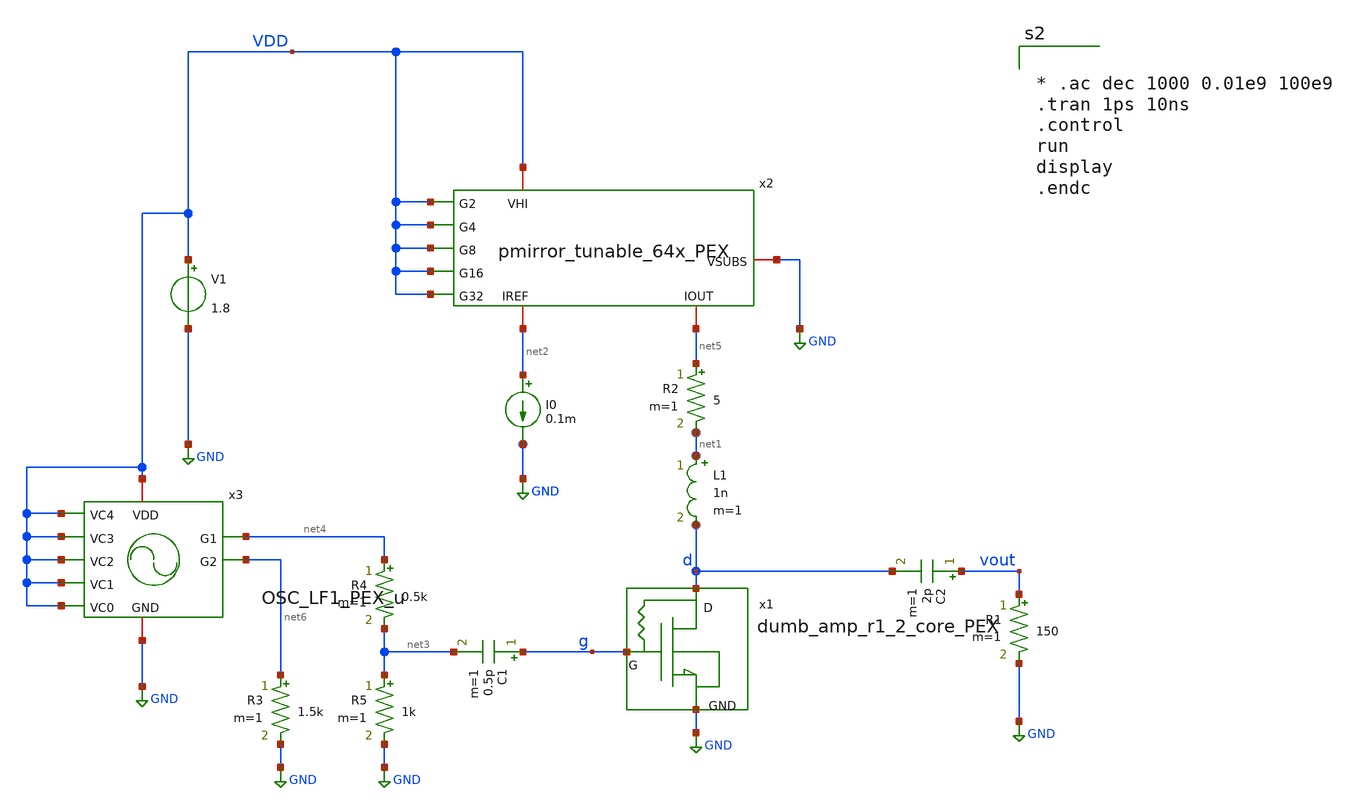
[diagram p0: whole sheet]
** sch_path: xschem/dumb_amp_r1_2_PEX_tran.sch
**.subckt dumb_amp_r1_2_PEX_tran
V1 VDD GND 1.8
C2 vout d 2p m=1
L1 net1 d 1n m=1
R2 net5 net1 5 m=1
I0 net2 GND 0.1m
R1 vout GND 150 m=1
R4 net4 net3 0.5k m=1
R5 net3 GND 1k m=1
x1 g d GND dumb_amp_r1_2_core_PEX
x2 VDD VDD VDD GND VDD net2 net5 VDD VDD pmirror_tunable_64x_PEX
C1 g net3 0.5p m=1
x3 VDD VDD net4 net6 VDD VDD VDD VDD GND OSC_LF1_PEX_u
R3 net6 GND 1.5k m=1
**** begin user architecture code
.lib $::SKYWATER_MODELS/sky130.lib.spice tt
* .include $::PDKPATH/libs.ref/sky130_fd_sc_hvl/spice/sky130_fd_sc_hvl.spice



* .ac dec 1000 0.01e9 100e9
.tran 1ps 10ns
.control
run
display
.endc


**** end user architecture code
**.ends

* expanding   symbol:  dumb_amp_r1_2_core_PEX.sym # of pins=3
** sym_path: xschem/dumb_amp_r1_2_core_PEX.sym
** sch_path: xschem/dumb_amp_r1_2_core_PEX.sch
.subckt dumb_amp_r1_2_core_PEX G D GND
*.iopin G
*.iopin D
*.iopin GND
**** begin user architecture code

.subckt dumb_amp_core_pex NGATE NDRAIN VSUBS
.subckt sky130_fd_pr__rf_nfet_01v8_aM02W5p00L0p15 DRAIN GATE SOURCE SUBSTRATE
X0 DRAIN GATE SOURCE SUBSTRATE sky130_fd_pr__nfet_01v8 ad=1.414e+12p pd=1.066e+07u as=2.828e+12p
+ ps=2.132e+07u w=5.05e+06u l=150000u
X1 SOURCE GATE DRAIN SUBSTRATE sky130_fd_pr__nfet_01v8 ad=0p pd=0u as=0p ps=0u w=5.05e+06u l=150000u
C0 DRAIN SOURCE 3.59fF
C1 GATE SOURCE 0.46fF
C2 DRAIN GATE 0.34fF
C3 DRAIN SUBSTRATE 0.40fF
C4 SOURCE SUBSTRATE 2.44fF
C5 GATE SUBSTRATE 0.64fF
.ends
.subckt nfet_3x_2 D G S sub
Xsky130_fd_pr__rf_nfet_01v8_aM02W5p00L0p15_0 D G S sub sky130_fd_pr__rf_nfet_01v8_aM02W5p00L0p15
Xsky130_fd_pr__rf_nfet_01v8_aM02W5p00L0p15_1 D G S sub sky130_fd_pr__rf_nfet_01v8_aM02W5p00L0p15
Xsky130_fd_pr__rf_nfet_01v8_aM02W5p00L0p15_2 D G S sub sky130_fd_pr__rf_nfet_01v8_aM02W5p00L0p15
C0 G sub 1.34fF
C1 S D -0.11fF
C2 S G 2.13fF
C3 G D 1.69fF
C4 S sub -0.01fF
C5 D sub -0.05fF
C6 sub 0 -1.34fF
C7 D 0 0.62fF
C8 S 0 6.66fF
C9 G 0 1.96fF
.ends
.subckt RF_nfet_6xaM02W5p0L0p15 G S D B
Xnfet_3x_2_0 D G S B nfet_3x_2
Xnfet_3x_2_1 D G S B nfet_3x_2
C0 D B -0.02fF
C1 G S 0.20fF
C2 G B 0.06fF
C3 G D 0.14fF
C4 S B 0.02fF
C5 D S 0.01fF
C6 B 0 -3.73fF
C7 D 0 1.02fF
C8 S 0 13.03fF
C9 G 0 3.30fF
.ends
.subckt sky130_fd_pr__res_generic_po_JFYRVD a_75_284# a_n141_n357# a_n271_n487#
R0 a_n141_n357# a_75_284# sky130_fd_pr__res_generic_po w=330000u l=6.2e+06u
C0 a_n141_n357# a_n271_n487# 0.14fF
C1 a_75_284# a_n271_n487# 0.14fF
.ends
XRF_nfet_6xaM02W5p0L0p15_0 NGATE NDRAIN VSUBS VSUBS RF_nfet_6xaM02W5p0L0p15
Xsky130_fd_pr__res_generic_po_JFYRVD_0 NGATE NDRAIN VSUBS sky130_fd_pr__res_generic_po_JFYRVD
C0 VSUBS NDRAIN 1.42fF
C1 NGATE VSUBS 2.81fF
C2 NGATE NDRAIN 2.91fF
C5 NDRAIN VSUBS 14.22fF
C6 NGATE VSUBS 3.28fF
.ends

XDUT G D GND dumb_amp_core_pex


**** end user architecture code
.ends


* expanding   symbol:  pmirror_tunable_64x_PEX.sym # of pins=9
** sym_path: xschem/pmirror_tunable_64x_PEX.sym
** sch_path: xschem/pmirror_tunable_64x_PEX.sch
.subckt pmirror_tunable_64x_PEX VHI G2 G4 VSUBS G8 IREF IOUT G16 G32
*.ipin G2
*.ipin G4
*.ipin G8
*.ipin G16
*.ipin G32
*.iopin VHI
*.iopin VSUBS
*.iopin IREF
*.iopin IOUT
**** begin user architecture code

* SPICE3 file created from pmirror_pfet_64x_complete.ext - technology: sky130B
X0 pmirror_pfet_64x_flat_0/G32 IREF VSUBS sky130_fd_pr__res_xhigh_po_0p35 l=500000u
X1 pmirror_pfet_64x_flat_0/G4  IREF VSUBS sky130_fd_pr__res_xhigh_po_0p35 l=500000u
X2 pmirror_pfet_64x_flat_0/G8  IREF VSUBS sky130_fd_pr__res_xhigh_po_0p35 l=500000u
X3 pmirror_pfet_64x_flat_0/G2  IREF VSUBS sky130_fd_pr__res_xhigh_po_0p35 l=500000u
X5 pmirror_pfet_64x_flat_0/G16 IREF VSUBS sky130_fd_pr__res_xhigh_po_0p35 l=500000u

X7 VHI pmirror_pfet_64x_flat_0/G32 IOUT VHI sky130_fd_pr__pfet_01v8 ad=0p pd=0u as=0p ps=0u w=1e+06u
+ l=300000u
X8 IOUT pmirror_pfet_64x_flat_0/G32 VHI VHI sky130_fd_pr__pfet_01v8 ad=0p pd=0u as=0p ps=0u w=1e+06u
+ l=300000u
X11 IOUT pmirror_pfet_64x_flat_0/G32 VHI VHI sky130_fd_pr__pfet_01v8 ad=0p pd=0u as=0p ps=0u
+ w=1e+06u l=300000u
X16 VHI pmirror_pfet_64x_flat_0/G32 IOUT VHI sky130_fd_pr__pfet_01v8 ad=0p pd=0u as=0p ps=0u
+ w=1e+06u l=300000u
X17 VHI pmirror_pfet_64x_flat_0/G32 IOUT VHI sky130_fd_pr__pfet_01v8 ad=0p pd=0u as=0p ps=0u
+ w=1e+06u l=300000u
X18 VHI pmirror_pfet_64x_flat_0/G32 IOUT VHI sky130_fd_pr__pfet_01v8 ad=0p pd=0u as=0p ps=0u
+ w=1e+06u l=300000u
X21 IOUT pmirror_pfet_64x_flat_0/G32 VHI VHI sky130_fd_pr__pfet_01v8 ad=0p pd=0u as=0p ps=0u
+ w=1e+06u l=300000u
X22 IOUT pmirror_pfet_64x_flat_0/G32 VHI VHI sky130_fd_pr__pfet_01v8 ad=0p pd=0u as=0p ps=0u
+ w=1e+06u l=300000u
X27 IOUT pmirror_pfet_64x_flat_0/G32 VHI VHI sky130_fd_pr__pfet_01v8 ad=1p pd=0u as=0p ps=0u
+ w=1e+06u l=300000u
X28 IOUT pmirror_pfet_64x_flat_0/G32 VHI VHI sky130_fd_pr__pfet_01v8 ad=0p pd=0u as=0p ps=0u
+ w=1e+06u l=300000u
X29 VHI pmirror_pfet_64x_flat_0/G32 IOUT VHI sky130_fd_pr__pfet_01v8 ad=0p pd=0u as=0p ps=0u
+ w=1e+06u l=300000u
X25 VHI pmirror_pfet_64x_flat_0/G32 IOUT VHI sky130_fd_pr__pfet_01v8 ad=0p pd=0u as=0p ps=0u
+ w=1e+06u l=300000u
X35 VHI pmirror_pfet_64x_flat_0/G32 IOUT VHI sky130_fd_pr__pfet_01v8 ad=0p pd=0u as=0p ps=0u
+ w=1e+06u l=300000u
X38 VHI pmirror_pfet_64x_flat_0/G32 IOUT VHI sky130_fd_pr__pfet_01v8 ad=0p pd=0u as=0p ps=0u
+ w=1e+06u l=300000u
X41 VHI pmirror_pfet_64x_flat_0/G32 IOUT VHI sky130_fd_pr__pfet_01v8 ad=0p pd=0u as=0p ps=0u
+ w=1e+06u l=300000u
X43 IOUT pmirror_pfet_64x_flat_0/G32 VHI VHI sky130_fd_pr__pfet_01v8 ad=0p pd=0u as=0p ps=0u
+ w=1e+06u l=300000u
X44 IOUT pmirror_pfet_64x_flat_0/G32 VHI VHI sky130_fd_pr__pfet_01v8 ad=0p pd=0u as=0p ps=0u
+ w=1e+06u l=300000u
X46 VHI pmirror_pfet_64x_flat_0/G32 IOUT VHI sky130_fd_pr__pfet_01v8 ad=0p pd=0u as=0p ps=0u
+ w=1e+06u l=300000u
X54 VHI pmirror_pfet_64x_flat_0/G32 IOUT VHI sky130_fd_pr__pfet_01v8 ad=0p pd=0u as=0p ps=0u
+ w=1e+06u l=300000u
X55 IOUT pmirror_pfet_64x_flat_0/G32 VHI VHI sky130_fd_pr__pfet_01v8 ad=0p pd=0u as=0p ps=0u
+ w=1e+06u l=300000u
X56 IOUT pmirror_pfet_64x_flat_0/G32 VHI VHI sky130_fd_pr__pfet_01v8 ad=0p pd=0u as=0p ps=0u
+ w=1e+06u l=300000u
X60 IOUT pmirror_pfet_64x_flat_0/G32 VHI VHI sky130_fd_pr__pfet_01v8 ad=0p pd=0u as=0p ps=0u
+ w=1e+06u l=300000u
X61 IOUT pmirror_pfet_64x_flat_0/G32 VHI VHI sky130_fd_pr__pfet_01v8 ad=0p pd=0u as=0p ps=0u
+ w=1e+06u l=300000u
X62 VHI pmirror_pfet_64x_flat_0/G32 IOUT VHI sky130_fd_pr__pfet_01v8 ad=0p pd=0u as=0p ps=0u
+ w=1e+06u l=300000u
X67 IOUT pmirror_pfet_64x_flat_0/G32 VHI VHI sky130_fd_pr__pfet_01v8 ad=0p pd=0u as=0p ps=0u
+ w=1e+06u l=300000u
X68 IOUT pmirror_pfet_64x_flat_0/G32 VHI VHI sky130_fd_pr__pfet_01v8 ad=0p pd=0u as=0p ps=0u
+ w=1e+06u l=300000u
X50 VHI pmirror_pfet_64x_flat_0/G32 IOUT VHI sky130_fd_pr__pfet_01v8 ad=0p pd=0u as=0p ps=0u
+ w=1e+06u l=300000u
X73 VHI pmirror_pfet_64x_flat_0/G32 IOUT VHI sky130_fd_pr__pfet_01v8 ad=0p pd=0u as=0p ps=0u
+ w=1e+06u l=300000u
X74 IOUT pmirror_pfet_64x_flat_0/G32 VHI VHI sky130_fd_pr__pfet_01v8 ad=0p pd=0u as=0p ps=0u
+ w=1e+06u l=300000u
X75 IOUT pmirror_pfet_64x_flat_0/G32 VHI VHI sky130_fd_pr__pfet_01v8 ad=0p pd=0u as=0p ps=0u
+ w=1e+06u l=300000u
X69 VHI pmirror_pfet_64x_flat_0/G32 IOUT VHI sky130_fd_pr__pfet_01v8 ad=0p pd=0u as=0p ps=0u
+ w=1e+06u l=300000u
X81 VHI pmirror_pfet_64x_flat_0/G32 IOUT VHI sky130_fd_pr__pfet_01v8 ad=0p pd=0u as=0p ps=0u
+ w=1e+06u l=300000u

X49 VHI VHI IOUT VHI sky130_fd_pr__pfet_01v8 ad=0p pd=0u as=0p ps=0u w=1e+06u l=300000u
X79 IREF IREF VHI VHI sky130_fd_pr__pfet_01v8 ad=0p pd=0u as=0p ps=0u w=1e+06u l=300000u

X6 IOUT pmirror_pfet_64x_flat_0/G16 VHI VHI sky130_fd_pr__pfet_01v8 ad=0p pd=0u as=0p ps=0u w=1e+06u
+ l=300000u
X9 VHI pmirror_pfet_64x_flat_0/G16 IOUT VHI sky130_fd_pr__pfet_01v8 ad=0p pd=0u as=0p ps=0u w=1e+06u
+ l=300000u
X10 IOUT pmirror_pfet_64x_flat_0/G16 VHI VHI sky130_fd_pr__pfet_01v8 ad=0p pd=0u as=0p ps=0u
+ w=1e+06u l=300000u
X19 IOUT pmirror_pfet_64x_flat_0/G16 VHI VHI sky130_fd_pr__pfet_01v8 ad=0p pd=0u as=0p ps=0u
+ w=1e+06u l=300000u
X20 IOUT pmirror_pfet_64x_flat_0/G16 VHI VHI sky130_fd_pr__pfet_01v8 ad=0p pd=0u as=0p ps=0u
+ w=1e+06u l=300000u
X26 VHI pmirror_pfet_64x_flat_0/G16 IOUT VHI sky130_fd_pr__pfet_01v8 ad=0p pd=0u as=0p ps=0u
+ w=1e+06u l=300000u
X30 IOUT pmirror_pfet_64x_flat_0/G16 VHI VHI sky130_fd_pr__pfet_01v8 ad=0p pd=0u as=0p ps=0u
+ w=1e+06u l=300000u
X33 IOUT pmirror_pfet_64x_flat_0/G16 VHI VHI sky130_fd_pr__pfet_01v8 ad=0p pd=0u as=0p ps=0u
+ w=1e+06u l=300000u
X36 VHI pmirror_pfet_64x_flat_0/G16 IOUT VHI sky130_fd_pr__pfet_01v8 ad=0p pd=0u as=0p ps=0u
+ w=1e+06u l=300000u
X45 VHI pmirror_pfet_64x_flat_0/G16 IOUT VHI sky130_fd_pr__pfet_01v8 ad=0p pd=0u as=0p ps=0u
+ w=1e+06u l=300000u
X53 VHI pmirror_pfet_64x_flat_0/G16 IOUT VHI sky130_fd_pr__pfet_01v8 ad=0p pd=0u as=0p ps=0u
+ w=1e+06u l=300000u
X57 VHI pmirror_pfet_64x_flat_0/G16 IOUT VHI sky130_fd_pr__pfet_01v8 ad=0p pd=0u as=0p ps=0u
+ w=1e+06u l=300000u
X58 VHI pmirror_pfet_64x_flat_0/G16 IOUT VHI sky130_fd_pr__pfet_01v8 ad=0p pd=0u as=0p ps=0u
+ w=1e+06u l=300000u
X65 VHI pmirror_pfet_64x_flat_0/G16 IOUT VHI sky130_fd_pr__pfet_01v8 ad=0p pd=0u as=0p ps=0u
+ w=1e+06u l=300000u
X82 IOUT pmirror_pfet_64x_flat_0/G16 VHI VHI sky130_fd_pr__pfet_01v8 ad=0p pd=0u as=0p ps=0u
+ w=1e+06u l=300000u
X83 IOUT pmirror_pfet_64x_flat_0/G16 VHI VHI sky130_fd_pr__pfet_01v8 ad=0p pd=0u as=0p ps=0u
+ w=1e+06u l=300000u

X14 IOUT pmirror_pfet_64x_flat_0/G8 VHI VHI sky130_fd_pr__pfet_01v8 ad=0p pd=0u as=0p ps=0u w=1e+06u
+ l=300000u
X23 VHI pmirror_pfet_64x_flat_0/G8 IOUT VHI sky130_fd_pr__pfet_01v8 ad=0p pd=0u as=0p ps=0u w=1e+06u
+ l=300000u
X31 VHI pmirror_pfet_64x_flat_0/G8 IOUT VHI sky130_fd_pr__pfet_01v8 ad=0p pd=0u as=0p ps=0u w=1e+06u
+ l=300000u
X32 VHI pmirror_pfet_64x_flat_0/G8 IOUT VHI sky130_fd_pr__pfet_01v8 ad=0p pd=0u as=0p ps=0u w=1e+06u
+ l=300000u
X42 VHI pmirror_pfet_64x_flat_0/G8 IOUT VHI sky130_fd_pr__pfet_01v8 ad=0p pd=0u as=0p ps=0u w=1e+06u
+ l=300000u
X72 IOUT pmirror_pfet_64x_flat_0/G8 VHI VHI sky130_fd_pr__pfet_01v8 ad=0p pd=0u as=0p ps=0u w=1e+06u
+ l=300000u
X80 IOUT pmirror_pfet_64x_flat_0/G8 VHI VHI sky130_fd_pr__pfet_01v8 ad=0p pd=0u as=0p ps=0u w=1e+06u
+ l=300000u
X84 IOUT pmirror_pfet_64x_flat_0/G8 VHI VHI sky130_fd_pr__pfet_01v8 ad=0p pd=0u as=0p ps=0u w=1e+06u
+ l=300000u

X85 IOUT pmirror_pfet_64x_flat_0/G4 VHI VHI sky130_fd_pr__pfet_01v8 ad=0p pd=0u as=0p ps=0u w=1e+06u
+ l=300000u
X39 VHI pmirror_pfet_64x_flat_0/G4 IOUT VHI sky130_fd_pr__pfet_01v8 ad=0p pd=0u as=0p ps=0u w=1e+06u
+ l=300000u
X40 VHI pmirror_pfet_64x_flat_0/G4 IOUT VHI sky130_fd_pr__pfet_01v8 ad=0p pd=0u as=0p ps=0u w=1e+06u
+ l=300000u
X70 IOUT pmirror_pfet_64x_flat_0/G4 VHI VHI sky130_fd_pr__pfet_01v8 ad=0p pd=0u as=0p ps=0u w=1e+06u
+ l=300000u

X48 VHI pmirror_pfet_64x_flat_0/G2 IOUT VHI sky130_fd_pr__pfet_01v8 ad=0p pd=0u as=0p ps=0u w=1e+06u
+ l=300000u
X15 IOUT pmirror_pfet_64x_flat_0/G2 VHI VHI sky130_fd_pr__pfet_01v8 ad=0p pd=0u as=0p ps=0u w=1e+06u
+ l=300000u

X86 VHI G32 pmirror_pfet_64x_flat_0/G32 VHI sky130_fd_pr__pfet_01v8 ad=0p pd=0u as=0p ps=0u
+ w=30e+06u l=150000u
X87 VHI G16 pmirror_pfet_64x_flat_0/G16 VHI sky130_fd_pr__pfet_01v8 ad=0p pd=0u as=0p ps=0u
+ w=30e+06u l=150000u
X88 VHI G2 pmirror_pfet_64x_flat_0/G2 VHI sky130_fd_pr__pfet_01v8 ad=0p pd=0u as=0p ps=0u w=30e+06u
+ l=150000u
X89 VHI G4 pmirror_pfet_64x_flat_0/G4 VHI sky130_fd_pr__pfet_01v8 ad=0p pd=0u as=0p ps=0u w=30e+06u
+ l=150000u
X90 VHI G8 pmirror_pfet_64x_flat_0/G8 VHI sky130_fd_pr__pfet_01v8 ad=0p pd=0u as=0p ps=0u w=30e+06u
+ l=150000u

C0 VHI pmirror_pfet_64x_flat_0/G8 10.15fF
C1 pmirror_pfet_64x_flat_0/G16 IOUT 2.36fF
C2 pmirror_pfet_64x_flat_0/G4 VHI 4.30fF
C3 pmirror_pfet_64x_flat_0/G2 IREF 2.13fF
C4 pmirror_pfet_64x_flat_0/G16 pmirror_pfet_64x_flat_0/G8 4.66fF
C5 pmirror_pfet_64x_flat_0/G4 pmirror_pfet_64x_flat_0/G8 3.24fF
C6 pmirror_pfet_64x_flat_0/G2 VHI 4.48fF
C7 pmirror_pfet_64x_flat_0/G4 pmirror_pfet_64x_flat_0/G2 2.55fF
C8 VHI IREF 4.53fF
C9 VHI pmirror_pfet_64x_flat_0/G32 15.40fF
C10 IOUT pmirror_pfet_64x_flat_0/G32 5.39fF
C11 pmirror_pfet_64x_flat_0/G16 pmirror_pfet_64x_flat_0/G32 3.74fF
C12 VHI IOUT 24.04fF
C13 pmirror_pfet_64x_flat_0/G16 VHI 4.93fF
C14 VHI VSUBS 46.10fF


**** end user architecture code
.ends


* expanding   symbol:  OSC_LF1_PEX_u.sym # of pins=9
** sym_path: xschem/OSC_LF1_PEX_u.sym
** sch_path: xschem/OSC_LF1_PEX_u.sch
.subckt OSC_LF1_PEX_u VDD VC4 G1 G2 VC3 VC2 VC1 VC0 GND
*.ipin VC0
*.ipin VC1
*.ipin VC2
*.ipin VC3
*.ipin VC4
*.iopin GND
*.iopin VDD
*.opin G1
*.opin G2
**** begin user architecture code






**** COMPLETE *****

.subckt COMPLETE VH VL I1 I2 G0 G1 G2 G3 G4

.subckt sky130_fd_pr__rf_pfet_01v8_aF04W5p00L0p15 DRAIN GATE SOURCE
X0 DRAIN GATE SOURCE SOURCE sky130_fd_pr__pfet_01v8 ad=2.8e+12p pd=2.112e+07u as=4.05e+12p
+ ps=3.162e+07u w=5e+06u l=150000u
X1 SOURCE GATE DRAIN SOURCE sky130_fd_pr__pfet_01v8 ad=0p pd=0u as=0p ps=0u w=5e+06u l=150000u
X2 SOURCE GATE DRAIN SOURCE sky130_fd_pr__pfet_01v8 ad=0p pd=0u as=0p ps=0u w=5e+06u l=150000u
X3 DRAIN GATE SOURCE SOURCE sky130_fd_pr__pfet_01v8 ad=0p pd=0u as=0p ps=0u w=5e+06u l=150000u
C0 DRAIN SOURCE 6.07fF
.ends

X0 I2 G0 captuner_complete_2_0/sky130_fd_pr__rf_nfet_01v8_aM04W5p00L0p15_fingered_0/S VL
+ sky130_fd_pr__nfet_01v8 ad=0p pd=0u as=0p ps=0u w=5.05e+06u l=150000u
X1 I2 G0 captuner_complete_2_0/sky130_fd_pr__rf_nfet_01v8_aM04W5p00L0p15_fingered_0/S VL
+ sky130_fd_pr__nfet_01v8 ad=0p pd=0u as=0p ps=0u w=5.05e+06u l=150000u
X2 captuner_complete_2_0/sky130_fd_pr__rf_nfet_01v8_aM04W5p00L0p15_fingered_0/S G0 I2 VL
+ sky130_fd_pr__nfet_01v8 ad=0p pd=0u as=0p ps=0u w=5.05e+06u l=150000u
X3 captuner_complete_2_0/sky130_fd_pr__rf_nfet_01v8_aM04W5p00L0p15_fingered_0/S G0 I2 VL
+ sky130_fd_pr__nfet_01v8 ad=0p pd=0u as=0p ps=0u w=5.05e+06u l=150000u
X4 I2 G1 captuner_complete_2_0/sky130_fd_pr__rf_nfet_01v8_aM04W5p00L0p15_fingered_1/S VL
+ sky130_fd_pr__nfet_01v8 ad=0p pd=0u as=0p ps=0u w=5.05e+06u l=150000u
X5 I2 G1 captuner_complete_2_0/sky130_fd_pr__rf_nfet_01v8_aM04W5p00L0p15_fingered_1/S VL
+ sky130_fd_pr__nfet_01v8 ad=0p pd=0u as=0p ps=0u w=5.05e+06u l=150000u
X6 captuner_complete_2_0/sky130_fd_pr__rf_nfet_01v8_aM04W5p00L0p15_fingered_1/S G1 I2 VL
+ sky130_fd_pr__nfet_01v8 ad=0p pd=0u as=0p ps=0u w=5.05e+06u l=150000u
X7 captuner_complete_2_0/sky130_fd_pr__rf_nfet_01v8_aM04W5p00L0p15_fingered_1/S G1 I2 VL
+ sky130_fd_pr__nfet_01v8 ad=0p pd=0u as=0p ps=0u w=5.05e+06u l=150000u
X8 I2 G2 captuner_complete_2_0/sky130_fd_pr__rf_nfet_01v8_aM04W5p00L0p15_fingered_2/S VL
+ sky130_fd_pr__nfet_01v8 ad=0p pd=0u as=0p ps=0u w=5.05e+06u l=150000u
X9 I2 G2 captuner_complete_2_0/sky130_fd_pr__rf_nfet_01v8_aM04W5p00L0p15_fingered_2/S VL
+ sky130_fd_pr__nfet_01v8 ad=0p pd=0u as=0p ps=0u w=5.05e+06u l=150000u
X10 captuner_complete_2_0/sky130_fd_pr__rf_nfet_01v8_aM04W5p00L0p15_fingered_2/S G2 I2 VL
+ sky130_fd_pr__nfet_01v8 ad=0p pd=0u as=0p ps=0u w=5.05e+06u l=150000u
X11 captuner_complete_2_0/sky130_fd_pr__rf_nfet_01v8_aM04W5p00L0p15_fingered_2/S G2 I2 VL
+ sky130_fd_pr__nfet_01v8 ad=0p pd=0u as=0p ps=0u w=5.05e+06u l=150000u
X12 I2 G3 captuner_complete_2_0/sky130_fd_pr__rf_nfet_01v8_aM04W5p00L0p15_fingered_4/S VL
+ sky130_fd_pr__nfet_01v8 ad=0p pd=0u as=0p ps=0u w=5.05e+06u l=150000u
X13 I2 G3 captuner_complete_2_0/sky130_fd_pr__rf_nfet_01v8_aM04W5p00L0p15_fingered_4/S VL
+ sky130_fd_pr__nfet_01v8 ad=0p pd=0u as=0p ps=0u w=5.05e+06u l=150000u
X14 captuner_complete_2_0/sky130_fd_pr__rf_nfet_01v8_aM04W5p00L0p15_fingered_4/S G3 I2 VL
+ sky130_fd_pr__nfet_01v8 ad=0p pd=0u as=0p ps=0u w=5.05e+06u l=150000u
X15 captuner_complete_2_0/sky130_fd_pr__rf_nfet_01v8_aM04W5p00L0p15_fingered_4/S G3 I2 VL
+ sky130_fd_pr__nfet_01v8 ad=0p pd=0u as=0p ps=0u w=5.05e+06u l=150000u
X16 I2 G3 captuner_complete_2_0/sky130_fd_pr__rf_nfet_01v8_aM04W5p00L0p15_fingered_4/S VL
+ sky130_fd_pr__nfet_01v8 ad=0p pd=0u as=0p ps=0u w=5.05e+06u l=150000u
X17 I2 G3 captuner_complete_2_0/sky130_fd_pr__rf_nfet_01v8_aM04W5p00L0p15_fingered_4/S VL
+ sky130_fd_pr__nfet_01v8 ad=0p pd=0u as=0p ps=0u w=5.05e+06u l=150000u
X18 captuner_complete_2_0/sky130_fd_pr__rf_nfet_01v8_aM04W5p00L0p15_fingered_4/S G3 I2 VL
+ sky130_fd_pr__nfet_01v8 ad=0p pd=0u as=0p ps=0u w=5.05e+06u l=150000u
X19 captuner_complete_2_0/sky130_fd_pr__rf_nfet_01v8_aM04W5p00L0p15_fingered_4/S G3 I2 VL
+ sky130_fd_pr__nfet_01v8 ad=0p pd=0u as=0p ps=0u w=5.05e+06u l=150000u
X20 I2 G4 captuner_complete_2_0/sky130_fd_pr__rf_nfet_01v8_aM04W5p00L0p15_fingered_6/S VL
+ sky130_fd_pr__nfet_01v8 ad=0p pd=0u as=0p ps=0u w=5.05e+06u l=150000u
X21 I2 G4 captuner_complete_2_0/sky130_fd_pr__rf_nfet_01v8_aM04W5p00L0p15_fingered_6/S VL
+ sky130_fd_pr__nfet_01v8 ad=0p pd=0u as=0p ps=0u w=5.05e+06u l=150000u
X22 captuner_complete_2_0/sky130_fd_pr__rf_nfet_01v8_aM04W5p00L0p15_fingered_6/S G4 I2 VL
+ sky130_fd_pr__nfet_01v8 ad=0p pd=0u as=0p ps=0u w=5.05e+06u l=150000u
X23 captuner_complete_2_0/sky130_fd_pr__rf_nfet_01v8_aM04W5p00L0p15_fingered_6/S G4 I2 VL
+ sky130_fd_pr__nfet_01v8 ad=0p pd=0u as=0p ps=0u w=5.05e+06u l=150000u
X24 I2 G4 captuner_complete_2_0/sky130_fd_pr__rf_nfet_01v8_aM04W5p00L0p15_fingered_6/S VL
+ sky130_fd_pr__nfet_01v8 ad=0p pd=0u as=0p ps=0u w=5.05e+06u l=150000u
X25 I2 G4 captuner_complete_2_0/sky130_fd_pr__rf_nfet_01v8_aM04W5p00L0p15_fingered_6/S VL
+ sky130_fd_pr__nfet_01v8 ad=0p pd=0u as=0p ps=0u w=5.05e+06u l=150000u
X26 captuner_complete_2_0/sky130_fd_pr__rf_nfet_01v8_aM04W5p00L0p15_fingered_6/S G4 I2 VL
+ sky130_fd_pr__nfet_01v8 ad=0p pd=0u as=0p ps=0u w=5.05e+06u l=150000u
X27 captuner_complete_2_0/sky130_fd_pr__rf_nfet_01v8_aM04W5p00L0p15_fingered_6/S G4 I2 VL
+ sky130_fd_pr__nfet_01v8 ad=0p pd=0u as=0p ps=0u w=5.05e+06u l=150000u
X28 I1 captuner_complete_2_0/sky130_fd_pr__rf_nfet_01v8_aM04W5p00L0p15_fingered_4/S
+ sky130_fd_pr__cap_mim_m3_1 l=4e+06u w=1e+07u
X29 I1 captuner_complete_2_0/sky130_fd_pr__rf_nfet_01v8_aM04W5p00L0p15_fingered_0/S
+ sky130_fd_pr__cap_mim_m3_1 l=1e+06u w=5e+06u
X30 I1 captuner_complete_2_0/sky130_fd_pr__rf_nfet_01v8_aM04W5p00L0p15_fingered_6/S
+ sky130_fd_pr__cap_mim_m3_1 l=8e+06u w=1e+07u
X31 I1 captuner_complete_2_0/sky130_fd_pr__rf_nfet_01v8_aM04W5p00L0p15_fingered_1/S
+ sky130_fd_pr__cap_mim_m3_1 l=1e+06u w=1e+07u
X32 I1 captuner_complete_2_0/sky130_fd_pr__rf_nfet_01v8_aM04W5p00L0p15_fingered_2/S
+ sky130_fd_pr__cap_mim_m3_1 l=2e+06u w=1e+07u
X33 VL I1 I2 VL sky130_fd_pr__nfet_01v8 ad=0p pd=0u as=0p ps=0u w=5.05e+06u l=150000u
X34 VL I1 I2 VL sky130_fd_pr__nfet_01v8 ad=0p pd=0u as=0p ps=0u w=5.05e+06u l=150000u
X35 I2 I1 VL VL sky130_fd_pr__nfet_01v8 ad=0p pd=0u as=0p ps=0u w=5.05e+06u l=150000u
X36 I2 I1 VL VL sky130_fd_pr__nfet_01v8 ad=0p pd=0u as=0p ps=0u w=5.05e+06u l=150000u
X37 VL I1 I2 VL sky130_fd_pr__nfet_01v8 ad=0p pd=0u as=0p ps=0u w=5.05e+06u l=150000u
X38 VL I1 I2 VL sky130_fd_pr__nfet_01v8 ad=0p pd=0u as=0p ps=0u w=5.05e+06u l=150000u
X39 I2 I1 VL VL sky130_fd_pr__nfet_01v8 ad=0p pd=0u as=0p ps=0u w=5.05e+06u l=150000u
X40 I2 I1 VL VL sky130_fd_pr__nfet_01v8 ad=0p pd=0u as=0p ps=0u w=5.05e+06u l=150000u
X41 VL I1 I2 VL sky130_fd_pr__nfet_01v8 ad=0p pd=0u as=0p ps=0u w=5.05e+06u l=150000u
X42 VL I1 I2 VL sky130_fd_pr__nfet_01v8 ad=0p pd=0u as=0p ps=0u w=5.05e+06u l=150000u
X43 I2 I1 VL VL sky130_fd_pr__nfet_01v8 ad=0p pd=0u as=0p ps=0u w=5.05e+06u l=150000u
X44 I2 I1 VL VL sky130_fd_pr__nfet_01v8 ad=0p pd=0u as=0p ps=0u w=5.05e+06u l=150000u
X45 VL I2 I1 VL sky130_fd_pr__nfet_01v8 ad=0p pd=0u as=0p ps=0u w=5.05e+06u l=150000u
X46 VL I2 I1 VL sky130_fd_pr__nfet_01v8 ad=0p pd=0u as=0p ps=0u w=5.05e+06u l=150000u
X47 I1 I2 VL VL sky130_fd_pr__nfet_01v8 ad=0p pd=0u as=0p ps=0u w=5.05e+06u l=150000u
X48 I1 I2 VL VL sky130_fd_pr__nfet_01v8 ad=0p pd=0u as=0p ps=0u w=5.05e+06u l=150000u
X49 VL I2 I1 VL sky130_fd_pr__nfet_01v8 ad=0p pd=0u as=0p ps=0u w=5.05e+06u l=150000u
X50 VL I2 I1 VL sky130_fd_pr__nfet_01v8 ad=0p pd=0u as=0p ps=0u w=5.05e+06u l=150000u
X51 I1 I2 VL VL sky130_fd_pr__nfet_01v8 ad=0p pd=0u as=0p ps=0u w=5.05e+06u l=150000u
X52 I1 I2 VL VL sky130_fd_pr__nfet_01v8 ad=0p pd=0u as=0p ps=0u w=5.05e+06u l=150000u
X53 VL I2 I1 VL sky130_fd_pr__nfet_01v8 ad=0p pd=0u as=0p ps=0u w=5.05e+06u l=150000u
X54 VL I2 I1 VL sky130_fd_pr__nfet_01v8 ad=0p pd=0u as=0p ps=0u w=5.05e+06u l=150000u
X55 I1 I2 VL VL sky130_fd_pr__nfet_01v8 ad=0p pd=0u as=0p ps=0u w=5.05e+06u l=150000u
X56 I1 I2 VL VL sky130_fd_pr__nfet_01v8 ad=0p pd=0u as=0p ps=0u w=5.05e+06u l=150000u
C0 captuner_complete_2_0/sky130_fd_pr__rf_nfet_01v8_aM04W5p00L0p15_fingered_2/S I2 10.36fF
C1 captuner_complete_2_0/sky130_fd_pr__rf_nfet_01v8_aM04W5p00L0p15_fingered_2/S I1 2.57fF
C2 I2 captuner_complete_2_0/sky130_fd_pr__rf_nfet_01v8_aM04W5p00L0p15_fingered_4/S 20.62fF
C3 I1 captuner_complete_2_0/sky130_fd_pr__rf_nfet_01v8_aM04W5p00L0p15_fingered_4/S 4.41fF
C4 G4 I2 2.69fF
C5 captuner_complete_2_0/sky130_fd_pr__rf_nfet_01v8_aM04W5p00L0p15_fingered_0/S I2 10.35fF
C6 I2 captuner_complete_2_0/sky130_fd_pr__rf_nfet_01v8_aM04W5p00L0p15_fingered_6/S 21.16fF
C7 captuner_complete_2_0/sky130_fd_pr__rf_nfet_01v8_aM04W5p00L0p15_fingered_1/S I2 10.32fF
C8 I1 captuner_complete_2_0/sky130_fd_pr__rf_nfet_01v8_aM04W5p00L0p15_fingered_6/S 8.73fF
C9 VH I2 56.20fF
C10 VH I1 56.69fF
C11 I2 I1 20.88fF
C12 I2 G3 2.54fF
Xsky130_fd_pr__cap_vpp_08p6x07p8_m1m2m3_shieldl1_0 VL VH VL
+ sky130_fd_pr__cap_vpp_08p6x07p8_m1m2m3_shieldl1
Xsky130_fd_pr__cap_vpp_08p6x07p8_m1m2m3_shieldl1_1 VL VH VL
+ sky130_fd_pr__cap_vpp_08p6x07p8_m1m2m3_shieldl1
Xsky130_fd_pr__cap_vpp_08p6x07p8_m1m2m3_shieldl1_2 VL VH VL
+ sky130_fd_pr__cap_vpp_08p6x07p8_m1m2m3_shieldl1
XXCP_1_0/RF_pfet_28xW5p0L0p15_0/sky130_fd_pr__rf_pfet_01v8_aF04W5p00L0p15_0 I2 I1  VH
+ sky130_fd_pr__rf_pfet_01v8_aF04W5p00L0p15
XXCP_1_0/RF_pfet_28xW5p0L0p15_0/sky130_fd_pr__rf_pfet_01v8_aF04W5p00L0p15_1 I2 I1  VH
+ sky130_fd_pr__rf_pfet_01v8_aF04W5p00L0p15
XXCP_1_0/RF_pfet_28xW5p0L0p15_0/sky130_fd_pr__rf_pfet_01v8_aF04W5p00L0p15_2 I2 I1  VH
+ sky130_fd_pr__rf_pfet_01v8_aF04W5p00L0p15
XXCP_1_0/RF_pfet_28xW5p0L0p15_0/sky130_fd_pr__rf_pfet_01v8_aF04W5p00L0p15_3 I2 I1  VH
+ sky130_fd_pr__rf_pfet_01v8_aF04W5p00L0p15
XXCP_1_0/RF_pfet_28xW5p0L0p15_0/sky130_fd_pr__rf_pfet_01v8_aF04W5p00L0p15_4 I2 I1  VH
+ sky130_fd_pr__rf_pfet_01v8_aF04W5p00L0p15
XXCP_1_0/RF_pfet_28xW5p0L0p15_0/sky130_fd_pr__rf_pfet_01v8_aF04W5p00L0p15_5 I2 I1  VH
+ sky130_fd_pr__rf_pfet_01v8_aF04W5p00L0p15
XXCP_1_0/RF_pfet_28xW5p0L0p15_0/sky130_fd_pr__rf_pfet_01v8_aF04W5p00L0p15_6 I2 I1  VH
+ sky130_fd_pr__rf_pfet_01v8_aF04W5p00L0p15
XXCP_1_0/RF_pfet_28xW5p0L0p15_1/sky130_fd_pr__rf_pfet_01v8_aF04W5p00L0p15_0 I1 I2  VH
+ sky130_fd_pr__rf_pfet_01v8_aF04W5p00L0p15
XXCP_1_0/RF_pfet_28xW5p0L0p15_1/sky130_fd_pr__rf_pfet_01v8_aF04W5p00L0p15_1 I1 I2  VH
+ sky130_fd_pr__rf_pfet_01v8_aF04W5p00L0p15
XXCP_1_0/RF_pfet_28xW5p0L0p15_1/sky130_fd_pr__rf_pfet_01v8_aF04W5p00L0p15_2 I1 I2  VH
+ sky130_fd_pr__rf_pfet_01v8_aF04W5p00L0p15
XXCP_1_0/RF_pfet_28xW5p0L0p15_1/sky130_fd_pr__rf_pfet_01v8_aF04W5p00L0p15_3 I1 I2  VH
+ sky130_fd_pr__rf_pfet_01v8_aF04W5p00L0p15
XXCP_1_0/RF_pfet_28xW5p0L0p15_1/sky130_fd_pr__rf_pfet_01v8_aF04W5p00L0p15_4 I1 I2  VH
+ sky130_fd_pr__rf_pfet_01v8_aF04W5p00L0p15
XXCP_1_0/RF_pfet_28xW5p0L0p15_1/sky130_fd_pr__rf_pfet_01v8_aF04W5p00L0p15_5 I1 I2  VH
+ sky130_fd_pr__rf_pfet_01v8_aF04W5p00L0p15
XXCP_1_0/RF_pfet_28xW5p0L0p15_1/sky130_fd_pr__rf_pfet_01v8_aF04W5p00L0p15_6 I1 I2  VH
+ sky130_fd_pr__rf_pfet_01v8_aF04W5p00L0p15
Xsky130_fd_pr__cap_vpp_08p6x07p8_m1m2m3_shieldl1_3 VL VH VL
+ sky130_fd_pr__cap_vpp_08p6x07p8_m1m2m3_shieldl1
C13 I1 VL 29.45fF
C14 I2 VL 45.54fF
C15 VH VL 543.94fF
C16 captuner_complete_2_0/sky130_fd_pr__rf_nfet_01v8_aM04W5p00L0p15_fingered_6/S VL 6.47fF
C17 G4 VL 5.45fF
C18 captuner_complete_2_0/sky130_fd_pr__rf_nfet_01v8_aM04W5p00L0p15_fingered_4/S VL 2.68fF
C19 G3 VL 4.98fF
C20 G2 VL 3.01fF
C21 G1 VL 2.97fF
C22 G0 VL 3.07fF

.ends

**** Instantiate ****

* XU_XCP VDD GND G1 G2 XCP
* XU_CAPTUNE G1 G2 GND VC0 VC1 VC2 VC3 VC4 CAPTUNE

XU_COMPLETE VDD GND G1 G2 VC0 VC1 VC2 VC3 VC4 COMPLETE




**** end user architecture code
I1 VDD G1 PULSE(0 10n 1n 10p 10p 1n 2)
L1 G2 net1 1.939n m=1
R1 net1 G1 9.6 m=1
.ends

.GLOBAL GND
.end
